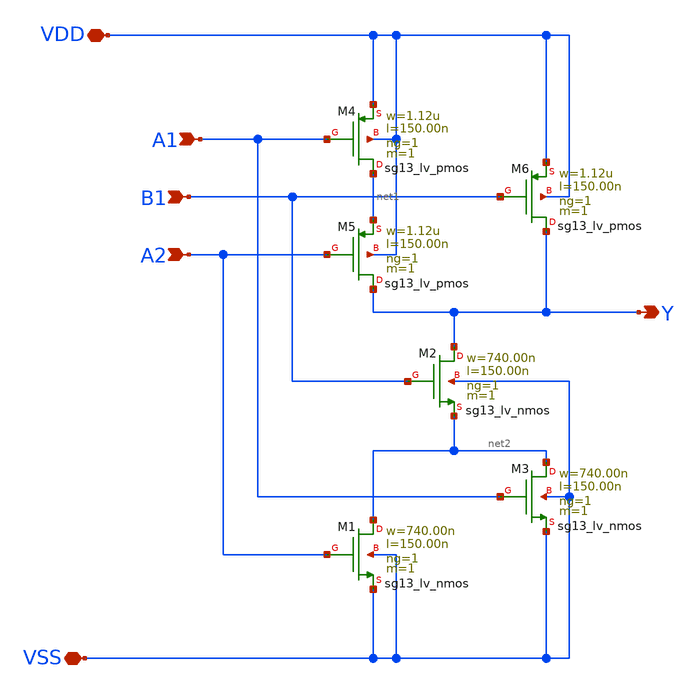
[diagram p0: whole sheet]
** sch_path: ihp-sg13g2/libs.tech/xschem/sg13g2_stdcells/sg13g2_o21ai_1.sch
**.subckt sg13g2_o21ai_1 A1 A2 B1 Y VDD VSS
*.ipin A1
*.ipin A2
*.ipin B1
*.opin Y
*.iopin VDD
*.iopin VSS
XM1 net2 A2 VSS VSS sg13_lv_nmos w=740.00n l=150.00n ng=1 m=1 mm_ok=1
XM2 Y B1 net2 VSS sg13_lv_nmos w=740.00n l=150.00n ng=1 m=1 mm_ok=1
XM3 net2 A1 VSS VSS sg13_lv_nmos w=740.00n l=150.00n ng=1 m=1 mm_ok=1
XM4 net1 A1 VDD VDD sg13_lv_pmos w=1.12u l=150.00n ng=1 m=1 mm_ok=1
XM5 Y A2 net1 VDD sg13_lv_pmos w=1.12u l=150.00n ng=1 m=1 mm_ok=1
XM6 Y B1 VDD VDD sg13_lv_pmos w=1.12u l=150.00n ng=1 m=1 mm_ok=1
**.ends
.end
